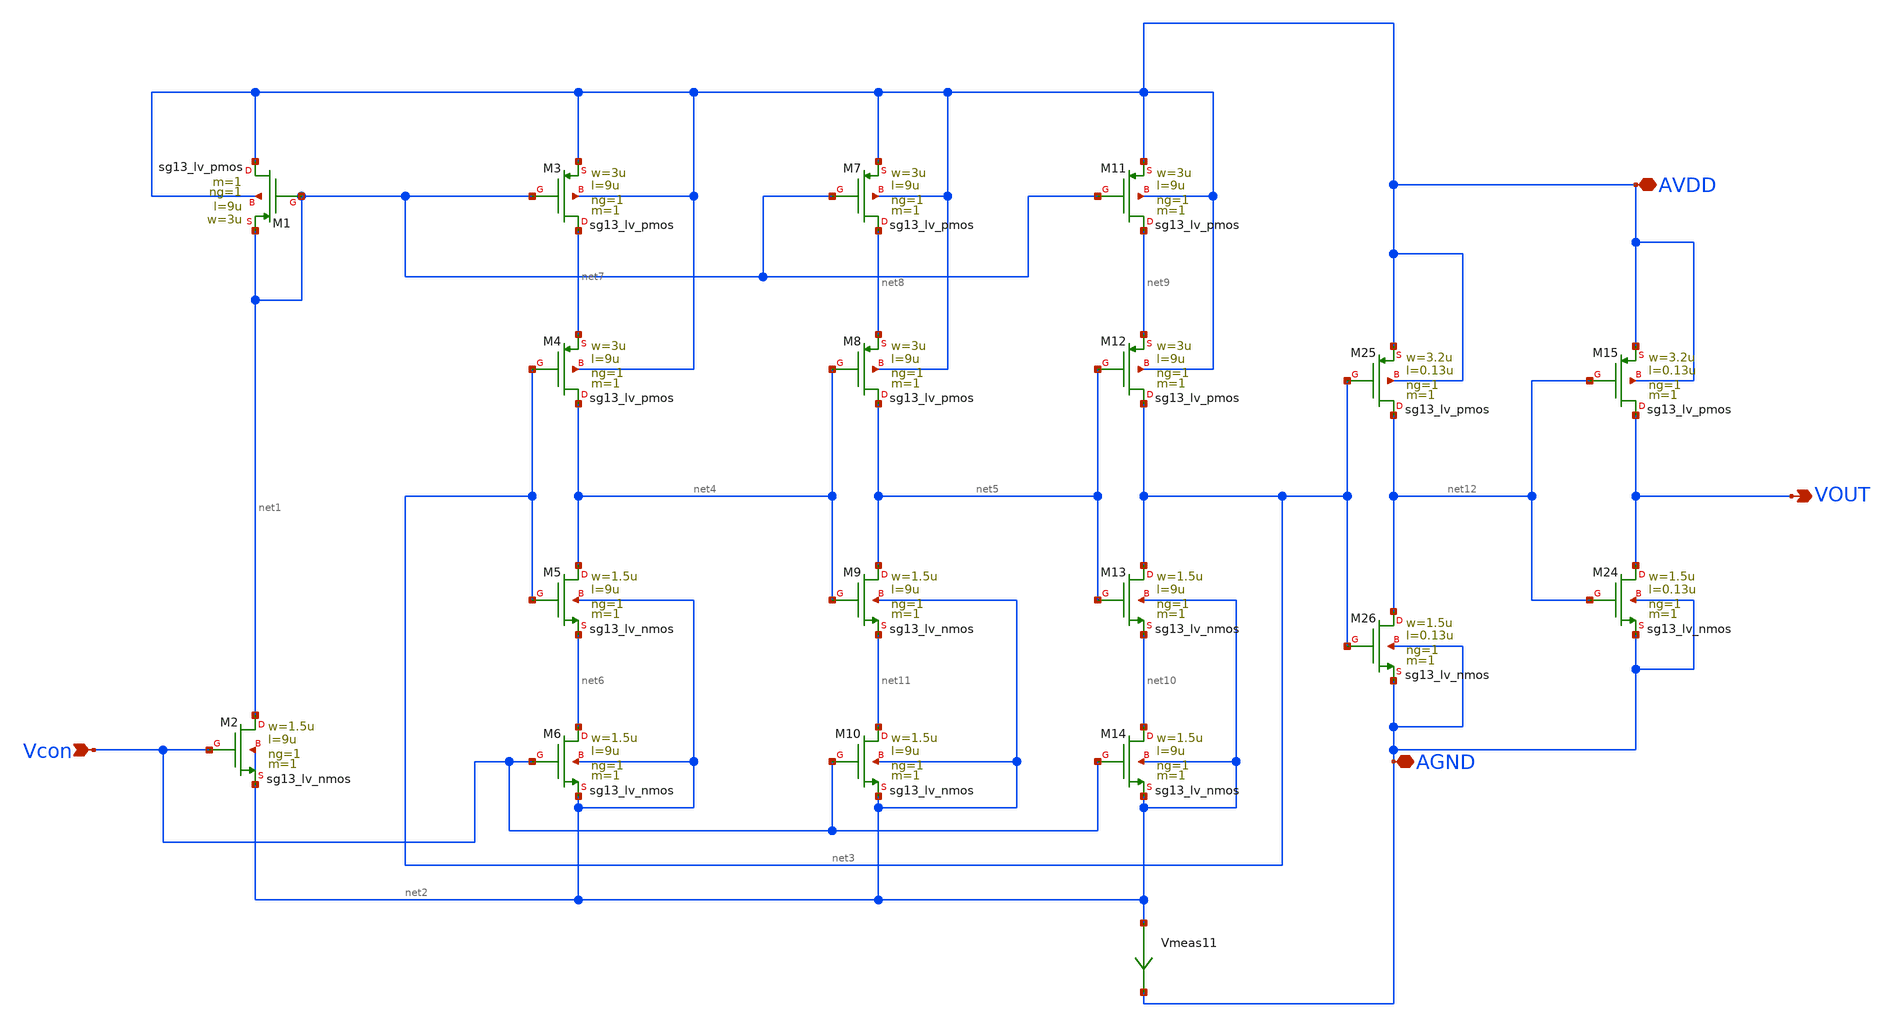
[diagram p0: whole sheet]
** sch_path: dependencies/VCO/VCO-main/netlist/layout/VCO.sch
**.subckt VCO Vcon AVDD AGND VOUT
*.ipin Vcon
*.iopin AVDD
*.iopin AGND
*.opin VOUT
XM2 net1 Vcon net2 net2 sg13_lv_nmos w=1.5u l=9u ng=1 m=1 mm_ok=1
XM3 net7 net1 AVDD AVDD sg13_lv_pmos w=3u l=9u ng=1 m=1 mm_ok=1
XM4 net4 net3 net7 AVDD sg13_lv_pmos w=3u l=9u ng=1 m=1 mm_ok=1
XM5 net4 net3 net6 net2 sg13_lv_nmos w=1.5u l=9u ng=1 m=1 mm_ok=1
XM6 net6 Vcon net2 net2 sg13_lv_nmos w=1.5u l=9u ng=1 m=1 mm_ok=1
XM7 net8 net1 AVDD AVDD sg13_lv_pmos w=3u l=9u ng=1 m=1 mm_ok=1
XM8 net5 net4 net8 AVDD sg13_lv_pmos w=3u l=9u ng=1 m=1 mm_ok=1
XM9 net5 net4 net11 net2 sg13_lv_nmos w=1.5u l=9u ng=1 m=1 mm_ok=1
XM10 net11 Vcon net2 net2 sg13_lv_nmos w=1.5u l=9u ng=1 m=1 mm_ok=1
XM11 net9 net1 AVDD AVDD sg13_lv_pmos w=3u l=9u ng=1 m=1 mm_ok=1
XM12 net3 net5 net9 AVDD sg13_lv_pmos w=3u l=9u ng=1 m=1 mm_ok=1
XM13 net3 net5 net10 net2 sg13_lv_nmos w=1.5u l=9u ng=1 m=1 mm_ok=1
XM14 net10 Vcon net2 net2 sg13_lv_nmos w=1.5u l=9u ng=1 m=1 mm_ok=1
XM1 AVDD net1 net1 AVDD sg13_lv_pmos w=3u l=9u ng=1 m=1 mm_ok=1
Vmeas11 net2 AGND 0
.save i(vmeas11)
XM24 VOUT net12 AGND AGND sg13_lv_nmos w=1.5u l=0.13u ng=1 m=1 mm_ok=1
XM25 net12 net3 AVDD AVDD sg13_lv_pmos w=3.2u l=0.13u ng=1 m=1 mm_ok=1
XM26 net12 net3 AGND AGND sg13_lv_nmos w=1.5u l=0.13u ng=1 m=1 mm_ok=1
XM15 VOUT net12 AVDD AVDD sg13_lv_pmos w=3.2u l=0.13u ng=1 m=1 mm_ok=1
**.ends
.end
